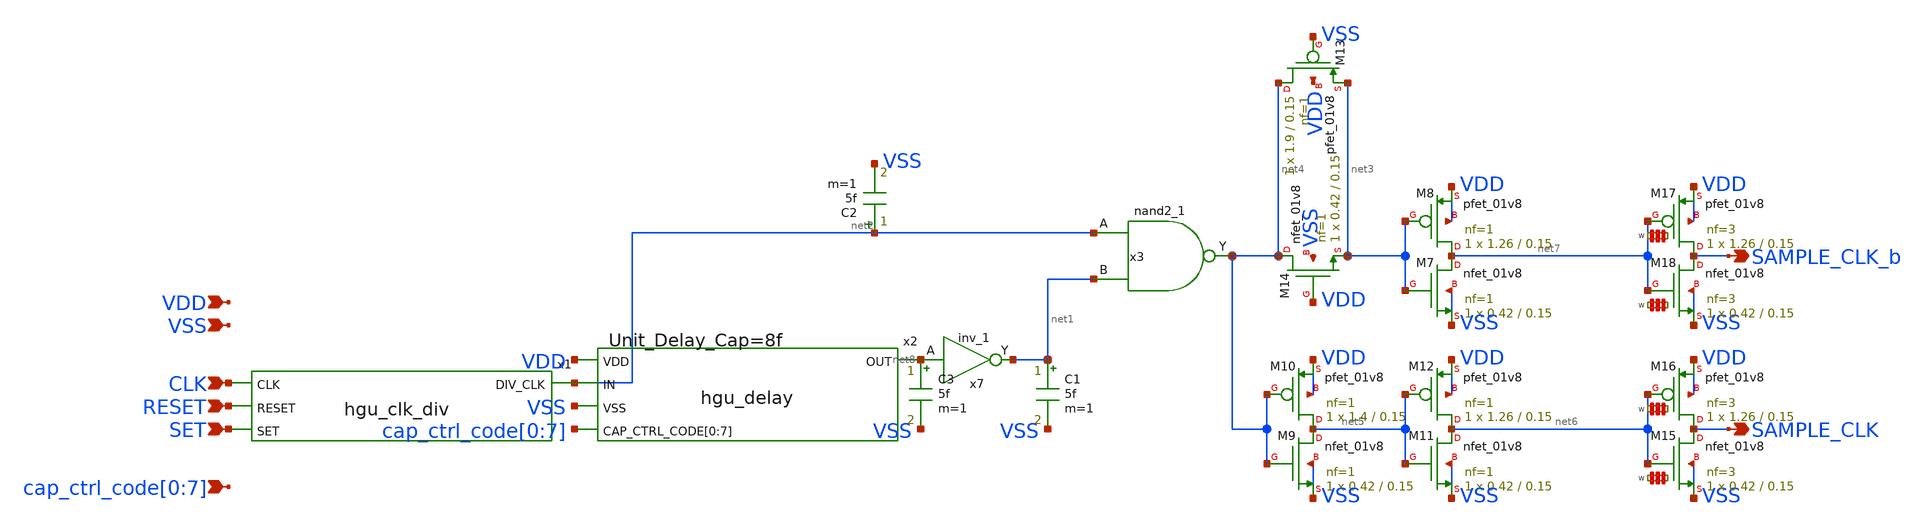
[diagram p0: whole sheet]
** sch_path: hgu/xschem/hgu_clk_sample.sch
**.subckt hgu_clk_sample VDD VSS SET RESET CLK
*+ cap_ctrl_code[0],cap_ctrl_code[1],cap_ctrl_code[2],cap_ctrl_code[3],cap_ctrl_code[4],cap_ctrl_code[5],cap_ctrl_code[6],cap_ctrl_code[7] SAMPLE_CLK SAMPLE_CLK_b
*.ipin VDD
*.ipin VSS
*.ipin SET
*.ipin RESET
*.ipin CLK
*.ipin
*+ cap_ctrl_code[0],cap_ctrl_code[1],cap_ctrl_code[2],cap_ctrl_code[3],cap_ctrl_code[4],cap_ctrl_code[5],cap_ctrl_code[6],cap_ctrl_code[7]
*.opin SAMPLE_CLK
*.opin SAMPLE_CLK_b
x1 net2 CLK RESET SET hgu_clk_div
x2 VDD net2 net8 VSS cap_ctrl_code[0] cap_ctrl_code[1] cap_ctrl_code[2] cap_ctrl_code[3]
+ cap_ctrl_code[4] cap_ctrl_code[5] cap_ctrl_code[6] cap_ctrl_code[7] hgu_delay DELAY_CAP=8f
x7 net8 VGND VNB VPB VPWR net1 sky130_fd_sc_hd__inv_1
C1 net1 VSS 5f m=1
C2 net2 VSS 5f m=1
C3 net8 VSS 5f m=1
x3 net2 net1 VGND VNB VPB VPWR net4 sky130_fd_sc_hd__nand2_1
XM7 net7 net3 VSS VSS sky130_fd_pr__nfet_01v8 L=0.15 W=0.42 nf=1 ad='int((nf+1)/2) * W/nf * 0.29' as='int((nf+2)/2) * W/nf * 0.29'
+ pd='2*int((nf+1)/2) * (W/nf + 0.29)' ps='2*int((nf+2)/2) * (W/nf + 0.29)' nrd='0.29 / W' nrs='0.29 / W'
+ sa=0 sb=0 sd=0 mult=1 m=1
XM8 net7 net3 VDD VDD sky130_fd_pr__pfet_01v8 L=0.15 W=1.26 nf=1 ad='int((nf+1)/2) * W/nf * 0.29' as='int((nf+2)/2) * W/nf * 0.29'
+ pd='2*int((nf+1)/2) * (W/nf + 0.29)' ps='2*int((nf+2)/2) * (W/nf + 0.29)' nrd='0.29 / W' nrs='0.29 / W'
+ sa=0 sb=0 sd=0 mult=1 m=1
XM9 net5 net4 VSS VSS sky130_fd_pr__nfet_01v8 L=0.15 W=0.42 nf=1 ad='int((nf+1)/2) * W/nf * 0.29' as='int((nf+2)/2) * W/nf * 0.29'
+ pd='2*int((nf+1)/2) * (W/nf + 0.29)' ps='2*int((nf+2)/2) * (W/nf + 0.29)' nrd='0.29 / W' nrs='0.29 / W'
+ sa=0 sb=0 sd=0 mult=1 m=1
XM10 net5 net4 VDD VDD sky130_fd_pr__pfet_01v8 L=0.15 W=1.4 nf=1 ad='int((nf+1)/2) * W/nf * 0.29' as='int((nf+2)/2) * W/nf * 0.29'
+ pd='2*int((nf+1)/2) * (W/nf + 0.29)' ps='2*int((nf+2)/2) * (W/nf + 0.29)' nrd='0.29 / W' nrs='0.29 / W'
+ sa=0 sb=0 sd=0 mult=1 m=1
XM11 net6 net5 VSS VSS sky130_fd_pr__nfet_01v8 L=0.15 W=0.42 nf=1 ad='int((nf+1)/2) * W/nf * 0.29' as='int((nf+2)/2) * W/nf * 0.29'
+ pd='2*int((nf+1)/2) * (W/nf + 0.29)' ps='2*int((nf+2)/2) * (W/nf + 0.29)' nrd='0.29 / W' nrs='0.29 / W'
+ sa=0 sb=0 sd=0 mult=1 m=1
XM12 net6 net5 VDD VDD sky130_fd_pr__pfet_01v8 L=0.15 W=1.26 nf=1 ad='int((nf+1)/2) * W/nf * 0.29' as='int((nf+2)/2) * W/nf * 0.29'
+ pd='2*int((nf+1)/2) * (W/nf + 0.29)' ps='2*int((nf+2)/2) * (W/nf + 0.29)' nrd='0.29 / W' nrs='0.29 / W'
+ sa=0 sb=0 sd=0 mult=1 m=1
XM13 net4 VSS net3 VDD sky130_fd_pr__pfet_01v8 L=0.15 W=1.9 nf=1 ad='int((nf+1)/2) * W/nf * 0.29' as='int((nf+2)/2) * W/nf * 0.29'
+ pd='2*int((nf+1)/2) * (W/nf + 0.29)' ps='2*int((nf+2)/2) * (W/nf + 0.29)' nrd='0.29 / W' nrs='0.29 / W'
+ sa=0 sb=0 sd=0 mult=1 m=1
XM14 net4 VDD net3 VSS sky130_fd_pr__nfet_01v8 L=0.15 W=0.42 nf=1 ad='int((nf+1)/2) * W/nf * 0.29' as='int((nf+2)/2) * W/nf * 0.29'
+ pd='2*int((nf+1)/2) * (W/nf + 0.29)' ps='2*int((nf+2)/2) * (W/nf + 0.29)' nrd='0.29 / W' nrs='0.29 / W'
+ sa=0 sb=0 sd=0 mult=1 m=1
XM15 SAMPLE_CLK net6 VSS VSS sky130_fd_pr__nfet_01v8 L=0.15 W='0.42 * 3 ' nf=3 ad='int((nf+1)/2) * W / nf * 0.29'
+ as='int((nf+2)/2) * W / nf * 0.29' pd='2*int((nf+1)/2) * (W / nf + 0.29)' ps='2*int((nf+2)/2) * (W / nf + 0.29)'
+ nrd='0.29 / W ' nrs='0.29 / W ' sa=0 sb=0 sd=0 mult=1 m=1
XM16 SAMPLE_CLK net6 VDD VDD sky130_fd_pr__pfet_01v8 L=0.15 W='1.26 * 3 ' nf=3 ad='int((nf+1)/2) * W / nf * 0.29'
+ as='int((nf+2)/2) * W / nf * 0.29' pd='2*int((nf+1)/2) * (W / nf + 0.29)' ps='2*int((nf+2)/2) * (W / nf + 0.29)'
+ nrd='0.29 / W ' nrs='0.29 / W ' sa=0 sb=0 sd=0 mult=1 m=1
XM17 SAMPLE_CLK_b net7 VDD VDD sky130_fd_pr__pfet_01v8 L=0.15 W='1.26 * 3 ' nf=3 ad='int((nf+1)/2) * W / nf * 0.29'
+ as='int((nf+2)/2) * W / nf * 0.29' pd='2*int((nf+1)/2) * (W / nf + 0.29)' ps='2*int((nf+2)/2) * (W / nf + 0.29)'
+ nrd='0.29 / W ' nrs='0.29 / W ' sa=0 sb=0 sd=0 mult=1 m=1
XM18 SAMPLE_CLK_b net7 VSS VSS sky130_fd_pr__nfet_01v8 L=0.15 W='0.42 * 3 ' nf=3 ad='int((nf+1)/2) * W / nf * 0.29'
+ as='int((nf+2)/2) * W / nf * 0.29' pd='2*int((nf+1)/2) * (W / nf + 0.29)' ps='2*int((nf+2)/2) * (W / nf + 0.29)'
+ nrd='0.29 / W ' nrs='0.29 / W ' sa=0 sb=0 sd=0 mult=1 m=1
**.ends

* expanding   symbol:  ../xschem/hgu_clk_div.sym # of pins=4
** sym_path: hgu/xschem/hgu_clk_div.sym
** sch_path: hgu/xschem/hgu_clk_div.sch
.subckt hgu_clk_div DIV_CLK CLK RESET SET
*.opin DIV_CLK
*.ipin SET
*.ipin RESET
*.ipin CLK
x2 CLK D_loop net1 net2 VGND VNB VPB VPWR DIV_CLK D_loop sky130_fd_sc_hd__dfbbp_1
x3 SET VGND VNB VPB VPWR net2 sky130_fd_sc_hd__inv_1
x4 RESET VGND VNB VPB VPWR net1 sky130_fd_sc_hd__inv_1
.ends


* expanding   symbol:  ../xschem/hgu_delay.sym # of pins=5
** sym_path: hgu/xschem/hgu_delay.sym
** sch_path: hgu/xschem/hgu_delay.sch
.subckt hgu_delay VDD IN OUT VSS CAP_CTRL_CODE[0] CAP_CTRL_CODE[1] CAP_CTRL_CODE[2] CAP_CTRL_CODE[3]
+ CAP_CTRL_CODE[4] CAP_CTRL_CODE[5] CAP_CTRL_CODE[6] CAP_CTRL_CODE[7]  DELAY_CAP=DELAY_CAP
*.ipin IN
*.ipin VDD
*.ipin VSS
*.opin OUT
*.ipin
*+ CAP_CTRL_CODE[0],CAP_CTRL_CODE[1],CAP_CTRL_CODE[2],CAP_CTRL_CODE[3],CAP_CTRL_CODE[4],CAP_CTRL_CODE[5],CAP_CTRL_CODE[6],CAP_CTRL_CODE[7]
XM1 net1 IN VSS VSS sky130_fd_pr__nfet_01v8 L=3.69 W=0.42 nf=1 ad='int((nf+1)/2) * W/nf * 0.29' as='int((nf+2)/2) * W/nf * 0.29'
+ pd='2*int((nf+1)/2) * (W/nf + 0.29)' ps='2*int((nf+2)/2) * (W/nf + 0.29)' nrd='0.29 / W' nrs='0.29 / W'
+ sa=0 sb=0 sd=0 mult=1 m=1
XM2 net1 IN VDD VDD sky130_fd_pr__pfet_01v8 L=1.5 W=0.8 nf=1 ad='int((nf+1)/2) * W/nf * 0.29' as='int((nf+2)/2) * W/nf * 0.29'
+ pd='2*int((nf+1)/2) * (W/nf + 0.29)' ps='2*int((nf+2)/2) * (W/nf + 0.29)' nrd='0.29 / W' nrs='0.29 / W'
+ sa=0 sb=0 sd=0 mult=1 m=1
XM3 VSS net1 VSS VSS sky130_fd_pr__nfet_01v8 L=2.045 W=1.375 nf=1 ad='int((nf+1)/2) * W/nf * 0.29' as='int((nf+2)/2) * W/nf * 0.29'
+ pd='2*int((nf+1)/2) * (W/nf + 0.29)' ps='2*int((nf+2)/2) * (W/nf + 0.29)' nrd='0.29 / W' nrs='0.29 / W'
+ sa=0 sb=0 sd=0 mult=1 m=1
XM4 OUT net1 net3 VSS sky130_fd_pr__nfet_01v8 L=0.15 W=0.42 nf=1 ad='int((nf+1)/2) * W/nf * 0.29' as='int((nf+2)/2) * W/nf * 0.29'
+ pd='2*int((nf+1)/2) * (W/nf + 0.29)' ps='2*int((nf+2)/2) * (W/nf + 0.29)' nrd='0.29 / W' nrs='0.29 / W'
+ sa=0 sb=0 sd=0 mult=1 m=1
XM5 OUT net1 net2 VDD sky130_fd_pr__pfet_01v8 L=0.15 W=0.8 nf=1 ad='int((nf+1)/2) * W/nf * 0.29' as='int((nf+2)/2) * W/nf * 0.29'
+ pd='2*int((nf+1)/2) * (W/nf + 0.29)' ps='2*int((nf+2)/2) * (W/nf + 0.29)' nrd='0.29 / W' nrs='0.29 / W'
+ sa=0 sb=0 sd=0 mult=1 m=1
XM6 net3 net1 VSS VSS sky130_fd_pr__nfet_01v8 L=0.15 W=0.42 nf=1 ad='int((nf+1)/2) * W/nf * 0.29' as='int((nf+2)/2) * W/nf * 0.29'
+ pd='2*int((nf+1)/2) * (W/nf + 0.29)' ps='2*int((nf+2)/2) * (W/nf + 0.29)' nrd='0.29 / W' nrs='0.29 / W'
+ sa=0 sb=0 sd=0 mult=1 m=1
XM7 net2 net1 VDD VDD sky130_fd_pr__pfet_01v8 L=0.15 W=0.8 nf=1 ad='int((nf+1)/2) * W/nf * 0.29' as='int((nf+2)/2) * W/nf * 0.29'
+ pd='2*int((nf+1)/2) * (W/nf + 0.29)' ps='2*int((nf+2)/2) * (W/nf + 0.29)' nrd='0.29 / W' nrs='0.29 / W'
+ sa=0 sb=0 sd=0 mult=1 m=1
XM8 VDD OUT net3 VSS sky130_fd_pr__nfet_01v8 L=0.15 W=0.84 nf=1 ad='int((nf+1)/2) * W/nf * 0.29' as='int((nf+2)/2) * W/nf * 0.29'
+ pd='2*int((nf+1)/2) * (W/nf + 0.29)' ps='2*int((nf+2)/2) * (W/nf + 0.29)' nrd='0.29 / W' nrs='0.29 / W'
+ sa=0 sb=0 sd=0 mult=1 m=1
XM9 VSS OUT net2 VDD sky130_fd_pr__pfet_01v8 L=0.15 W=1.6 nf=1 ad='int((nf+1)/2) * W/nf * 0.29' as='int((nf+2)/2) * W/nf * 0.29'
+ pd='2*int((nf+1)/2) * (W/nf + 0.29)' ps='2*int((nf+2)/2) * (W/nf + 0.29)' nrd='0.29 / W' nrs='0.29 / W'
+ sa=0 sb=0 sd=0 mult=1 m=1
x2 CAP_CTRL_CODE[0] VSS net1 hgu_sw_cap DELAY_CAP=DELAY_CAP
x3[1] CAP_CTRL_CODE[1] VSS net1 hgu_sw_cap DELAY_CAP=DELAY_CAP
x3[0] CAP_CTRL_CODE[1] VSS net1 hgu_sw_cap DELAY_CAP=DELAY_CAP
x4[3] CAP_CTRL_CODE[2] VSS net1 hgu_sw_cap DELAY_CAP=DELAY_CAP
x4[2] CAP_CTRL_CODE[2] VSS net1 hgu_sw_cap DELAY_CAP=DELAY_CAP
x4[1] CAP_CTRL_CODE[2] VSS net1 hgu_sw_cap DELAY_CAP=DELAY_CAP
x4[0] CAP_CTRL_CODE[2] VSS net1 hgu_sw_cap DELAY_CAP=DELAY_CAP
x5[7] CAP_CTRL_CODE[3] VSS net1 hgu_sw_cap DELAY_CAP=DELAY_CAP
x5[6] CAP_CTRL_CODE[3] VSS net1 hgu_sw_cap DELAY_CAP=DELAY_CAP
x5[5] CAP_CTRL_CODE[3] VSS net1 hgu_sw_cap DELAY_CAP=DELAY_CAP
x5[4] CAP_CTRL_CODE[3] VSS net1 hgu_sw_cap DELAY_CAP=DELAY_CAP
x5[3] CAP_CTRL_CODE[3] VSS net1 hgu_sw_cap DELAY_CAP=DELAY_CAP
x5[2] CAP_CTRL_CODE[3] VSS net1 hgu_sw_cap DELAY_CAP=DELAY_CAP
x5[1] CAP_CTRL_CODE[3] VSS net1 hgu_sw_cap DELAY_CAP=DELAY_CAP
x5[0] CAP_CTRL_CODE[3] VSS net1 hgu_sw_cap DELAY_CAP=DELAY_CAP
x6[15] CAP_CTRL_CODE[4] VSS net1 hgu_sw_cap DELAY_CAP=DELAY_CAP
x6[14] CAP_CTRL_CODE[4] VSS net1 hgu_sw_cap DELAY_CAP=DELAY_CAP
x6[13] CAP_CTRL_CODE[4] VSS net1 hgu_sw_cap DELAY_CAP=DELAY_CAP
x6[12] CAP_CTRL_CODE[4] VSS net1 hgu_sw_cap DELAY_CAP=DELAY_CAP
x6[11] CAP_CTRL_CODE[4] VSS net1 hgu_sw_cap DELAY_CAP=DELAY_CAP
x6[10] CAP_CTRL_CODE[4] VSS net1 hgu_sw_cap DELAY_CAP=DELAY_CAP
x6[9] CAP_CTRL_CODE[4] VSS net1 hgu_sw_cap DELAY_CAP=DELAY_CAP
x6[8] CAP_CTRL_CODE[4] VSS net1 hgu_sw_cap DELAY_CAP=DELAY_CAP
x6[7] CAP_CTRL_CODE[4] VSS net1 hgu_sw_cap DELAY_CAP=DELAY_CAP
x6[6] CAP_CTRL_CODE[4] VSS net1 hgu_sw_cap DELAY_CAP=DELAY_CAP
x6[5] CAP_CTRL_CODE[4] VSS net1 hgu_sw_cap DELAY_CAP=DELAY_CAP
x6[4] CAP_CTRL_CODE[4] VSS net1 hgu_sw_cap DELAY_CAP=DELAY_CAP
x6[3] CAP_CTRL_CODE[4] VSS net1 hgu_sw_cap DELAY_CAP=DELAY_CAP
x6[2] CAP_CTRL_CODE[4] VSS net1 hgu_sw_cap DELAY_CAP=DELAY_CAP
x6[1] CAP_CTRL_CODE[4] VSS net1 hgu_sw_cap DELAY_CAP=DELAY_CAP
x6[0] CAP_CTRL_CODE[4] VSS net1 hgu_sw_cap DELAY_CAP=DELAY_CAP
x7[31] CAP_CTRL_CODE[5] VSS net1 hgu_sw_cap DELAY_CAP=DELAY_CAP
x7[30] CAP_CTRL_CODE[5] VSS net1 hgu_sw_cap DELAY_CAP=DELAY_CAP
x7[29] CAP_CTRL_CODE[5] VSS net1 hgu_sw_cap DELAY_CAP=DELAY_CAP
x7[28] CAP_CTRL_CODE[5] VSS net1 hgu_sw_cap DELAY_CAP=DELAY_CAP
x7[27] CAP_CTRL_CODE[5] VSS net1 hgu_sw_cap DELAY_CAP=DELAY_CAP
x7[26] CAP_CTRL_CODE[5] VSS net1 hgu_sw_cap DELAY_CAP=DELAY_CAP
x7[25] CAP_CTRL_CODE[5] VSS net1 hgu_sw_cap DELAY_CAP=DELAY_CAP
x7[24] CAP_CTRL_CODE[5] VSS net1 hgu_sw_cap DELAY_CAP=DELAY_CAP
x7[23] CAP_CTRL_CODE[5] VSS net1 hgu_sw_cap DELAY_CAP=DELAY_CAP
x7[22] CAP_CTRL_CODE[5] VSS net1 hgu_sw_cap DELAY_CAP=DELAY_CAP
x7[21] CAP_CTRL_CODE[5] VSS net1 hgu_sw_cap DELAY_CAP=DELAY_CAP
x7[20] CAP_CTRL_CODE[5] VSS net1 hgu_sw_cap DELAY_CAP=DELAY_CAP
x7[19] CAP_CTRL_CODE[5] VSS net1 hgu_sw_cap DELAY_CAP=DELAY_CAP
x7[18] CAP_CTRL_CODE[5] VSS net1 hgu_sw_cap DELAY_CAP=DELAY_CAP
x7[17] CAP_CTRL_CODE[5] VSS net1 hgu_sw_cap DELAY_CAP=DELAY_CAP
x7[16] CAP_CTRL_CODE[5] VSS net1 hgu_sw_cap DELAY_CAP=DELAY_CAP
x7[15] CAP_CTRL_CODE[5] VSS net1 hgu_sw_cap DELAY_CAP=DELAY_CAP
x7[14] CAP_CTRL_CODE[5] VSS net1 hgu_sw_cap DELAY_CAP=DELAY_CAP
x7[13] CAP_CTRL_CODE[5] VSS net1 hgu_sw_cap DELAY_CAP=DELAY_CAP
x7[12] CAP_CTRL_CODE[5] VSS net1 hgu_sw_cap DELAY_CAP=DELAY_CAP
x7[11] CAP_CTRL_CODE[5] VSS net1 hgu_sw_cap DELAY_CAP=DELAY_CAP
x7[10] CAP_CTRL_CODE[5] VSS net1 hgu_sw_cap DELAY_CAP=DELAY_CAP
x7[9] CAP_CTRL_CODE[5] VSS net1 hgu_sw_cap DELAY_CAP=DELAY_CAP
x7[8] CAP_CTRL_CODE[5] VSS net1 hgu_sw_cap DELAY_CAP=DELAY_CAP
x7[7] CAP_CTRL_CODE[5] VSS net1 hgu_sw_cap DELAY_CAP=DELAY_CAP
x7[6] CAP_CTRL_CODE[5] VSS net1 hgu_sw_cap DELAY_CAP=DELAY_CAP
x7[5] CAP_CTRL_CODE[5] VSS net1 hgu_sw_cap DELAY_CAP=DELAY_CAP
x7[4] CAP_CTRL_CODE[5] VSS net1 hgu_sw_cap DELAY_CAP=DELAY_CAP
x7[3] CAP_CTRL_CODE[5] VSS net1 hgu_sw_cap DELAY_CAP=DELAY_CAP
x7[2] CAP_CTRL_CODE[5] VSS net1 hgu_sw_cap DELAY_CAP=DELAY_CAP
x7[1] CAP_CTRL_CODE[5] VSS net1 hgu_sw_cap DELAY_CAP=DELAY_CAP
x7[0] CAP_CTRL_CODE[5] VSS net1 hgu_sw_cap DELAY_CAP=DELAY_CAP
x8[63] CAP_CTRL_CODE[6] VSS net1 hgu_sw_cap DELAY_CAP=DELAY_CAP
x8[62] CAP_CTRL_CODE[6] VSS net1 hgu_sw_cap DELAY_CAP=DELAY_CAP
x8[61] CAP_CTRL_CODE[6] VSS net1 hgu_sw_cap DELAY_CAP=DELAY_CAP
x8[60] CAP_CTRL_CODE[6] VSS net1 hgu_sw_cap DELAY_CAP=DELAY_CAP
x8[59] CAP_CTRL_CODE[6] VSS net1 hgu_sw_cap DELAY_CAP=DELAY_CAP
x8[58] CAP_CTRL_CODE[6] VSS net1 hgu_sw_cap DELAY_CAP=DELAY_CAP
x8[57] CAP_CTRL_CODE[6] VSS net1 hgu_sw_cap DELAY_CAP=DELAY_CAP
x8[56] CAP_CTRL_CODE[6] VSS net1 hgu_sw_cap DELAY_CAP=DELAY_CAP
x8[55] CAP_CTRL_CODE[6] VSS net1 hgu_sw_cap DELAY_CAP=DELAY_CAP
x8[54] CAP_CTRL_CODE[6] VSS net1 hgu_sw_cap DELAY_CAP=DELAY_CAP
x8[53] CAP_CTRL_CODE[6] VSS net1 hgu_sw_cap DELAY_CAP=DELAY_CAP
x8[52] CAP_CTRL_CODE[6] VSS net1 hgu_sw_cap DELAY_CAP=DELAY_CAP
x8[51] CAP_CTRL_CODE[6] VSS net1 hgu_sw_cap DELAY_CAP=DELAY_CAP
x8[50] CAP_CTRL_CODE[6] VSS net1 hgu_sw_cap DELAY_CAP=DELAY_CAP
x8[49] CAP_CTRL_CODE[6] VSS net1 hgu_sw_cap DELAY_CAP=DELAY_CAP
x8[48] CAP_CTRL_CODE[6] VSS net1 hgu_sw_cap DELAY_CAP=DELAY_CAP
x8[47] CAP_CTRL_CODE[6] VSS net1 hgu_sw_cap DELAY_CAP=DELAY_CAP
x8[46] CAP_CTRL_CODE[6] VSS net1 hgu_sw_cap DELAY_CAP=DELAY_CAP
x8[45] CAP_CTRL_CODE[6] VSS net1 hgu_sw_cap DELAY_CAP=DELAY_CAP
x8[44] CAP_CTRL_CODE[6] VSS net1 hgu_sw_cap DELAY_CAP=DELAY_CAP
x8[43] CAP_CTRL_CODE[6] VSS net1 hgu_sw_cap DELAY_CAP=DELAY_CAP
x8[42] CAP_CTRL_CODE[6] VSS net1 hgu_sw_cap DELAY_CAP=DELAY_CAP
x8[41] CAP_CTRL_CODE[6] VSS net1 hgu_sw_cap DELAY_CAP=DELAY_CAP
x8[40] CAP_CTRL_CODE[6] VSS net1 hgu_sw_cap DELAY_CAP=DELAY_CAP
x8[39] CAP_CTRL_CODE[6] VSS net1 hgu_sw_cap DELAY_CAP=DELAY_CAP
x8[38] CAP_CTRL_CODE[6] VSS net1 hgu_sw_cap DELAY_CAP=DELAY_CAP
x8[37] CAP_CTRL_CODE[6] VSS net1 hgu_sw_cap DELAY_CAP=DELAY_CAP
x8[36] CAP_CTRL_CODE[6] VSS net1 hgu_sw_cap DELAY_CAP=DELAY_CAP
x8[35] CAP_CTRL_CODE[6] VSS net1 hgu_sw_cap DELAY_CAP=DELAY_CAP
x8[34] CAP_CTRL_CODE[6] VSS net1 hgu_sw_cap DELAY_CAP=DELAY_CAP
x8[33] CAP_CTRL_CODE[6] VSS net1 hgu_sw_cap DELAY_CAP=DELAY_CAP
x8[32] CAP_CTRL_CODE[6] VSS net1 hgu_sw_cap DELAY_CAP=DELAY_CAP
x8[31] CAP_CTRL_CODE[6] VSS net1 hgu_sw_cap DELAY_CAP=DELAY_CAP
x8[30] CAP_CTRL_CODE[6] VSS net1 hgu_sw_cap DELAY_CAP=DELAY_CAP
x8[29] CAP_CTRL_CODE[6] VSS net1 hgu_sw_cap DELAY_CAP=DELAY_CAP
x8[28] CAP_CTRL_CODE[6] VSS net1 hgu_sw_cap DELAY_CAP=DELAY_CAP
x8[27] CAP_CTRL_CODE[6] VSS net1 hgu_sw_cap DELAY_CAP=DELAY_CAP
x8[26] CAP_CTRL_CODE[6] VSS net1 hgu_sw_cap DELAY_CAP=DELAY_CAP
x8[25] CAP_CTRL_CODE[6] VSS net1 hgu_sw_cap DELAY_CAP=DELAY_CAP
x8[24] CAP_CTRL_CODE[6] VSS net1 hgu_sw_cap DELAY_CAP=DELAY_CAP
x8[23] CAP_CTRL_CODE[6] VSS net1 hgu_sw_cap DELAY_CAP=DELAY_CAP
x8[22] CAP_CTRL_CODE[6] VSS net1 hgu_sw_cap DELAY_CAP=DELAY_CAP
x8[21] CAP_CTRL_CODE[6] VSS net1 hgu_sw_cap DELAY_CAP=DELAY_CAP
x8[20] CAP_CTRL_CODE[6] VSS net1 hgu_sw_cap DELAY_CAP=DELAY_CAP
x8[19] CAP_CTRL_CODE[6] VSS net1 hgu_sw_cap DELAY_CAP=DELAY_CAP
x8[18] CAP_CTRL_CODE[6] VSS net1 hgu_sw_cap DELAY_CAP=DELAY_CAP
x8[17] CAP_CTRL_CODE[6] VSS net1 hgu_sw_cap DELAY_CAP=DELAY_CAP
x8[16] CAP_CTRL_CODE[6] VSS net1 hgu_sw_cap DELAY_CAP=DELAY_CAP
x8[15] CAP_CTRL_CODE[6] VSS net1 hgu_sw_cap DELAY_CAP=DELAY_CAP
x8[14] CAP_CTRL_CODE[6] VSS net1 hgu_sw_cap DELAY_CAP=DELAY_CAP
x8[13] CAP_CTRL_CODE[6] VSS net1 hgu_sw_cap DELAY_CAP=DELAY_CAP
x8[12] CAP_CTRL_CODE[6] VSS net1 hgu_sw_cap DELAY_CAP=DELAY_CAP
x8[11] CAP_CTRL_CODE[6] VSS net1 hgu_sw_cap DELAY_CAP=DELAY_CAP
x8[10] CAP_CTRL_CODE[6] VSS net1 hgu_sw_cap DELAY_CAP=DELAY_CAP
x8[9] CAP_CTRL_CODE[6] VSS net1 hgu_sw_cap DELAY_CAP=DELAY_CAP
x8[8] CAP_CTRL_CODE[6] VSS net1 hgu_sw_cap DELAY_CAP=DELAY_CAP
x8[7] CAP_CTRL_CODE[6] VSS net1 hgu_sw_cap DELAY_CAP=DELAY_CAP
x8[6] CAP_CTRL_CODE[6] VSS net1 hgu_sw_cap DELAY_CAP=DELAY_CAP
x8[5] CAP_CTRL_CODE[6] VSS net1 hgu_sw_cap DELAY_CAP=DELAY_CAP
x8[4] CAP_CTRL_CODE[6] VSS net1 hgu_sw_cap DELAY_CAP=DELAY_CAP
x8[3] CAP_CTRL_CODE[6] VSS net1 hgu_sw_cap DELAY_CAP=DELAY_CAP
x8[2] CAP_CTRL_CODE[6] VSS net1 hgu_sw_cap DELAY_CAP=DELAY_CAP
x8[1] CAP_CTRL_CODE[6] VSS net1 hgu_sw_cap DELAY_CAP=DELAY_CAP
x8[0] CAP_CTRL_CODE[6] VSS net1 hgu_sw_cap DELAY_CAP=DELAY_CAP
x1[127] CAP_CTRL_CODE[7] VSS net1 hgu_sw_cap DELAY_CAP=DELAY_CAP
x1[126] CAP_CTRL_CODE[7] VSS net1 hgu_sw_cap DELAY_CAP=DELAY_CAP
x1[125] CAP_CTRL_CODE[7] VSS net1 hgu_sw_cap DELAY_CAP=DELAY_CAP
x1[124] CAP_CTRL_CODE[7] VSS net1 hgu_sw_cap DELAY_CAP=DELAY_CAP
x1[123] CAP_CTRL_CODE[7] VSS net1 hgu_sw_cap DELAY_CAP=DELAY_CAP
x1[122] CAP_CTRL_CODE[7] VSS net1 hgu_sw_cap DELAY_CAP=DELAY_CAP
x1[121] CAP_CTRL_CODE[7] VSS net1 hgu_sw_cap DELAY_CAP=DELAY_CAP
x1[120] CAP_CTRL_CODE[7] VSS net1 hgu_sw_cap DELAY_CAP=DELAY_CAP
x1[119] CAP_CTRL_CODE[7] VSS net1 hgu_sw_cap DELAY_CAP=DELAY_CAP
x1[118] CAP_CTRL_CODE[7] VSS net1 hgu_sw_cap DELAY_CAP=DELAY_CAP
x1[117] CAP_CTRL_CODE[7] VSS net1 hgu_sw_cap DELAY_CAP=DELAY_CAP
x1[116] CAP_CTRL_CODE[7] VSS net1 hgu_sw_cap DELAY_CAP=DELAY_CAP
x1[115] CAP_CTRL_CODE[7] VSS net1 hgu_sw_cap DELAY_CAP=DELAY_CAP
x1[114] CAP_CTRL_CODE[7] VSS net1 hgu_sw_cap DELAY_CAP=DELAY_CAP
x1[113] CAP_CTRL_CODE[7] VSS net1 hgu_sw_cap DELAY_CAP=DELAY_CAP
x1[112] CAP_CTRL_CODE[7] VSS net1 hgu_sw_cap DELAY_CAP=DELAY_CAP
x1[111] CAP_CTRL_CODE[7] VSS net1 hgu_sw_cap DELAY_CAP=DELAY_CAP
x1[110] CAP_CTRL_CODE[7] VSS net1 hgu_sw_cap DELAY_CAP=DELAY_CAP
x1[109] CAP_CTRL_CODE[7] VSS net1 hgu_sw_cap DELAY_CAP=DELAY_CAP
x1[108] CAP_CTRL_CODE[7] VSS net1 hgu_sw_cap DELAY_CAP=DELAY_CAP
x1[107] CAP_CTRL_CODE[7] VSS net1 hgu_sw_cap DELAY_CAP=DELAY_CAP
x1[106] CAP_CTRL_CODE[7] VSS net1 hgu_sw_cap DELAY_CAP=DELAY_CAP
x1[105] CAP_CTRL_CODE[7] VSS net1 hgu_sw_cap DELAY_CAP=DELAY_CAP
x1[104] CAP_CTRL_CODE[7] VSS net1 hgu_sw_cap DELAY_CAP=DELAY_CAP
x1[103] CAP_CTRL_CODE[7] VSS net1 hgu_sw_cap DELAY_CAP=DELAY_CAP
x1[102] CAP_CTRL_CODE[7] VSS net1 hgu_sw_cap DELAY_CAP=DELAY_CAP
x1[101] CAP_CTRL_CODE[7] VSS net1 hgu_sw_cap DELAY_CAP=DELAY_CAP
x1[100] CAP_CTRL_CODE[7] VSS net1 hgu_sw_cap DELAY_CAP=DELAY_CAP
x1[99] CAP_CTRL_CODE[7] VSS net1 hgu_sw_cap DELAY_CAP=DELAY_CAP
x1[98] CAP_CTRL_CODE[7] VSS net1 hgu_sw_cap DELAY_CAP=DELAY_CAP
x1[97] CAP_CTRL_CODE[7] VSS net1 hgu_sw_cap DELAY_CAP=DELAY_CAP
x1[96] CAP_CTRL_CODE[7] VSS net1 hgu_sw_cap DELAY_CAP=DELAY_CAP
x1[95] CAP_CTRL_CODE[7] VSS net1 hgu_sw_cap DELAY_CAP=DELAY_CAP
x1[94] CAP_CTRL_CODE[7] VSS net1 hgu_sw_cap DELAY_CAP=DELAY_CAP
x1[93] CAP_CTRL_CODE[7] VSS net1 hgu_sw_cap DELAY_CAP=DELAY_CAP
x1[92] CAP_CTRL_CODE[7] VSS net1 hgu_sw_cap DELAY_CAP=DELAY_CAP
x1[91] CAP_CTRL_CODE[7] VSS net1 hgu_sw_cap DELAY_CAP=DELAY_CAP
x1[90] CAP_CTRL_CODE[7] VSS net1 hgu_sw_cap DELAY_CAP=DELAY_CAP
x1[89] CAP_CTRL_CODE[7] VSS net1 hgu_sw_cap DELAY_CAP=DELAY_CAP
x1[88] CAP_CTRL_CODE[7] VSS net1 hgu_sw_cap DELAY_CAP=DELAY_CAP
x1[87] CAP_CTRL_CODE[7] VSS net1 hgu_sw_cap DELAY_CAP=DELAY_CAP
x1[86] CAP_CTRL_CODE[7] VSS net1 hgu_sw_cap DELAY_CAP=DELAY_CAP
x1[85] CAP_CTRL_CODE[7] VSS net1 hgu_sw_cap DELAY_CAP=DELAY_CAP
x1[84] CAP_CTRL_CODE[7] VSS net1 hgu_sw_cap DELAY_CAP=DELAY_CAP
x1[83] CAP_CTRL_CODE[7] VSS net1 hgu_sw_cap DELAY_CAP=DELAY_CAP
x1[82] CAP_CTRL_CODE[7] VSS net1 hgu_sw_cap DELAY_CAP=DELAY_CAP
x1[81] CAP_CTRL_CODE[7] VSS net1 hgu_sw_cap DELAY_CAP=DELAY_CAP
x1[80] CAP_CTRL_CODE[7] VSS net1 hgu_sw_cap DELAY_CAP=DELAY_CAP
x1[79] CAP_CTRL_CODE[7] VSS net1 hgu_sw_cap DELAY_CAP=DELAY_CAP
x1[78] CAP_CTRL_CODE[7] VSS net1 hgu_sw_cap DELAY_CAP=DELAY_CAP
x1[77] CAP_CTRL_CODE[7] VSS net1 hgu_sw_cap DELAY_CAP=DELAY_CAP
x1[76] CAP_CTRL_CODE[7] VSS net1 hgu_sw_cap DELAY_CAP=DELAY_CAP
x1[75] CAP_CTRL_CODE[7] VSS net1 hgu_sw_cap DELAY_CAP=DELAY_CAP
x1[74] CAP_CTRL_CODE[7] VSS net1 hgu_sw_cap DELAY_CAP=DELAY_CAP
x1[73] CAP_CTRL_CODE[7] VSS net1 hgu_sw_cap DELAY_CAP=DELAY_CAP
x1[72] CAP_CTRL_CODE[7] VSS net1 hgu_sw_cap DELAY_CAP=DELAY_CAP
x1[71] CAP_CTRL_CODE[7] VSS net1 hgu_sw_cap DELAY_CAP=DELAY_CAP
x1[70] CAP_CTRL_CODE[7] VSS net1 hgu_sw_cap DELAY_CAP=DELAY_CAP
x1[69] CAP_CTRL_CODE[7] VSS net1 hgu_sw_cap DELAY_CAP=DELAY_CAP
x1[68] CAP_CTRL_CODE[7] VSS net1 hgu_sw_cap DELAY_CAP=DELAY_CAP
x1[67] CAP_CTRL_CODE[7] VSS net1 hgu_sw_cap DELAY_CAP=DELAY_CAP
x1[66] CAP_CTRL_CODE[7] VSS net1 hgu_sw_cap DELAY_CAP=DELAY_CAP
x1[65] CAP_CTRL_CODE[7] VSS net1 hgu_sw_cap DELAY_CAP=DELAY_CAP
x1[64] CAP_CTRL_CODE[7] VSS net1 hgu_sw_cap DELAY_CAP=DELAY_CAP
x1[63] CAP_CTRL_CODE[7] VSS net1 hgu_sw_cap DELAY_CAP=DELAY_CAP
x1[62] CAP_CTRL_CODE[7] VSS net1 hgu_sw_cap DELAY_CAP=DELAY_CAP
x1[61] CAP_CTRL_CODE[7] VSS net1 hgu_sw_cap DELAY_CAP=DELAY_CAP
x1[60] CAP_CTRL_CODE[7] VSS net1 hgu_sw_cap DELAY_CAP=DELAY_CAP
x1[59] CAP_CTRL_CODE[7] VSS net1 hgu_sw_cap DELAY_CAP=DELAY_CAP
x1[58] CAP_CTRL_CODE[7] VSS net1 hgu_sw_cap DELAY_CAP=DELAY_CAP
x1[57] CAP_CTRL_CODE[7] VSS net1 hgu_sw_cap DELAY_CAP=DELAY_CAP
x1[56] CAP_CTRL_CODE[7] VSS net1 hgu_sw_cap DELAY_CAP=DELAY_CAP
x1[55] CAP_CTRL_CODE[7] VSS net1 hgu_sw_cap DELAY_CAP=DELAY_CAP
x1[54] CAP_CTRL_CODE[7] VSS net1 hgu_sw_cap DELAY_CAP=DELAY_CAP
x1[53] CAP_CTRL_CODE[7] VSS net1 hgu_sw_cap DELAY_CAP=DELAY_CAP
x1[52] CAP_CTRL_CODE[7] VSS net1 hgu_sw_cap DELAY_CAP=DELAY_CAP
x1[51] CAP_CTRL_CODE[7] VSS net1 hgu_sw_cap DELAY_CAP=DELAY_CAP
x1[50] CAP_CTRL_CODE[7] VSS net1 hgu_sw_cap DELAY_CAP=DELAY_CAP
x1[49] CAP_CTRL_CODE[7] VSS net1 hgu_sw_cap DELAY_CAP=DELAY_CAP
x1[48] CAP_CTRL_CODE[7] VSS net1 hgu_sw_cap DELAY_CAP=DELAY_CAP
x1[47] CAP_CTRL_CODE[7] VSS net1 hgu_sw_cap DELAY_CAP=DELAY_CAP
x1[46] CAP_CTRL_CODE[7] VSS net1 hgu_sw_cap DELAY_CAP=DELAY_CAP
x1[45] CAP_CTRL_CODE[7] VSS net1 hgu_sw_cap DELAY_CAP=DELAY_CAP
x1[44] CAP_CTRL_CODE[7] VSS net1 hgu_sw_cap DELAY_CAP=DELAY_CAP
x1[43] CAP_CTRL_CODE[7] VSS net1 hgu_sw_cap DELAY_CAP=DELAY_CAP
x1[42] CAP_CTRL_CODE[7] VSS net1 hgu_sw_cap DELAY_CAP=DELAY_CAP
x1[41] CAP_CTRL_CODE[7] VSS net1 hgu_sw_cap DELAY_CAP=DELAY_CAP
x1[40] CAP_CTRL_CODE[7] VSS net1 hgu_sw_cap DELAY_CAP=DELAY_CAP
x1[39] CAP_CTRL_CODE[7] VSS net1 hgu_sw_cap DELAY_CAP=DELAY_CAP
x1[38] CAP_CTRL_CODE[7] VSS net1 hgu_sw_cap DELAY_CAP=DELAY_CAP
x1[37] CAP_CTRL_CODE[7] VSS net1 hgu_sw_cap DELAY_CAP=DELAY_CAP
x1[36] CAP_CTRL_CODE[7] VSS net1 hgu_sw_cap DELAY_CAP=DELAY_CAP
x1[35] CAP_CTRL_CODE[7] VSS net1 hgu_sw_cap DELAY_CAP=DELAY_CAP
x1[34] CAP_CTRL_CODE[7] VSS net1 hgu_sw_cap DELAY_CAP=DELAY_CAP
x1[33] CAP_CTRL_CODE[7] VSS net1 hgu_sw_cap DELAY_CAP=DELAY_CAP
x1[32] CAP_CTRL_CODE[7] VSS net1 hgu_sw_cap DELAY_CAP=DELAY_CAP
x1[31] CAP_CTRL_CODE[7] VSS net1 hgu_sw_cap DELAY_CAP=DELAY_CAP
x1[30] CAP_CTRL_CODE[7] VSS net1 hgu_sw_cap DELAY_CAP=DELAY_CAP
x1[29] CAP_CTRL_CODE[7] VSS net1 hgu_sw_cap DELAY_CAP=DELAY_CAP
x1[28] CAP_CTRL_CODE[7] VSS net1 hgu_sw_cap DELAY_CAP=DELAY_CAP
x1[27] CAP_CTRL_CODE[7] VSS net1 hgu_sw_cap DELAY_CAP=DELAY_CAP
x1[26] CAP_CTRL_CODE[7] VSS net1 hgu_sw_cap DELAY_CAP=DELAY_CAP
x1[25] CAP_CTRL_CODE[7] VSS net1 hgu_sw_cap DELAY_CAP=DELAY_CAP
x1[24] CAP_CTRL_CODE[7] VSS net1 hgu_sw_cap DELAY_CAP=DELAY_CAP
x1[23] CAP_CTRL_CODE[7] VSS net1 hgu_sw_cap DELAY_CAP=DELAY_CAP
x1[22] CAP_CTRL_CODE[7] VSS net1 hgu_sw_cap DELAY_CAP=DELAY_CAP
x1[21] CAP_CTRL_CODE[7] VSS net1 hgu_sw_cap DELAY_CAP=DELAY_CAP
x1[20] CAP_CTRL_CODE[7] VSS net1 hgu_sw_cap DELAY_CAP=DELAY_CAP
x1[19] CAP_CTRL_CODE[7] VSS net1 hgu_sw_cap DELAY_CAP=DELAY_CAP
x1[18] CAP_CTRL_CODE[7] VSS net1 hgu_sw_cap DELAY_CAP=DELAY_CAP
x1[17] CAP_CTRL_CODE[7] VSS net1 hgu_sw_cap DELAY_CAP=DELAY_CAP
x1[16] CAP_CTRL_CODE[7] VSS net1 hgu_sw_cap DELAY_CAP=DELAY_CAP
x1[15] CAP_CTRL_CODE[7] VSS net1 hgu_sw_cap DELAY_CAP=DELAY_CAP
x1[14] CAP_CTRL_CODE[7] VSS net1 hgu_sw_cap DELAY_CAP=DELAY_CAP
x1[13] CAP_CTRL_CODE[7] VSS net1 hgu_sw_cap DELAY_CAP=DELAY_CAP
x1[12] CAP_CTRL_CODE[7] VSS net1 hgu_sw_cap DELAY_CAP=DELAY_CAP
x1[11] CAP_CTRL_CODE[7] VSS net1 hgu_sw_cap DELAY_CAP=DELAY_CAP
x1[10] CAP_CTRL_CODE[7] VSS net1 hgu_sw_cap DELAY_CAP=DELAY_CAP
x1[9] CAP_CTRL_CODE[7] VSS net1 hgu_sw_cap DELAY_CAP=DELAY_CAP
x1[8] CAP_CTRL_CODE[7] VSS net1 hgu_sw_cap DELAY_CAP=DELAY_CAP
x1[7] CAP_CTRL_CODE[7] VSS net1 hgu_sw_cap DELAY_CAP=DELAY_CAP
x1[6] CAP_CTRL_CODE[7] VSS net1 hgu_sw_cap DELAY_CAP=DELAY_CAP
x1[5] CAP_CTRL_CODE[7] VSS net1 hgu_sw_cap DELAY_CAP=DELAY_CAP
x1[4] CAP_CTRL_CODE[7] VSS net1 hgu_sw_cap DELAY_CAP=DELAY_CAP
x1[3] CAP_CTRL_CODE[7] VSS net1 hgu_sw_cap DELAY_CAP=DELAY_CAP
x1[2] CAP_CTRL_CODE[7] VSS net1 hgu_sw_cap DELAY_CAP=DELAY_CAP
x1[1] CAP_CTRL_CODE[7] VSS net1 hgu_sw_cap DELAY_CAP=DELAY_CAP
x1[0] CAP_CTRL_CODE[7] VSS net1 hgu_sw_cap DELAY_CAP=DELAY_CAP
.ends


* expanding   symbol:  ../xschem/hgu_sw_cap.sym # of pins=3
** sym_path: hgu/xschem/hgu_sw_cap.sym
** sch_path: hgu/xschem/hgu_sw_cap.sch
.subckt hgu_sw_cap SW VSS DELAY_SIGNAL  DELAY_CAP=DELAY_CAP
*.ipin SW
*.ipin VSS
*.iopin DELAY_SIGNAL
XM14 DELAY_SIGNAL SW net1 VSS sky130_fd_pr__nfet_01v8 L=0.15 W=0.42 nf=1 ad='int((nf+1)/2) * W/nf * 0.29'
+ as='int((nf+2)/2) * W/nf * 0.29' pd='2*int((nf+1)/2) * (W/nf + 0.29)' ps='2*int((nf+2)/2) * (W/nf + 0.29)'
+ nrd='0.29 / W' nrs='0.29 / W' sa=0 sb=0 sd=0 mult=1 m=1
C1 net1 VSS 4.37f m=1
.ends

.end
